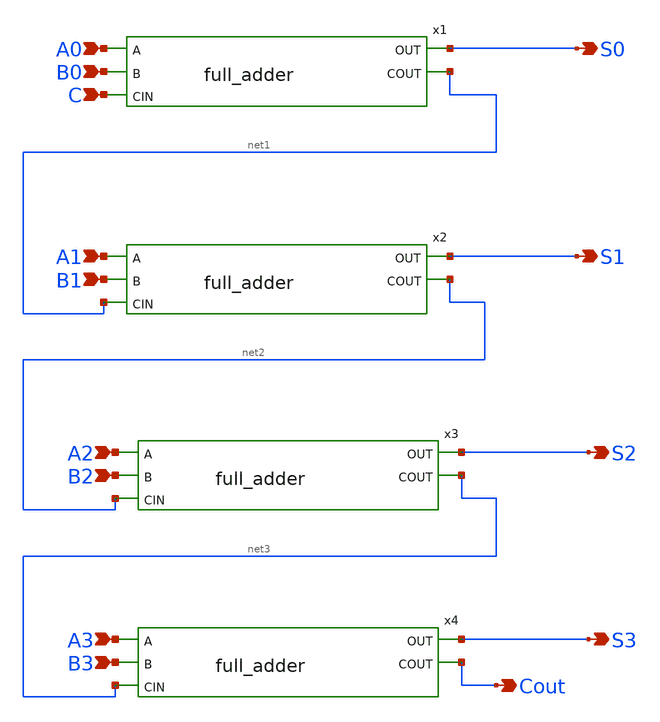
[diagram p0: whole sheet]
** sch_path: design/xschem/ADDER/4-bit_adder.sch
**.subckt 4-bit_adder C Cout S3 S0 S1 S2 A0 B0 A1 B1 A2 B2 A3 B3
*.ipin C
*.opin Cout
*.opin S3
*.opin S0
*.opin S1
*.opin S2
*.ipin A0
*.ipin B0
*.ipin A1
*.ipin B1
*.ipin A2
*.ipin B2
*.ipin A3
*.ipin B3
x1 S0 A0 B0 C net1 VSS VDD full_adder
x2 S1 A1 B1 net1 net2 VSS VDD full_adder
x3 S2 A2 B2 net2 net3 VSS VDD full_adder
x4 S3 A3 B3 net3 Cout VSS VDD full_adder
**.ends
.end
